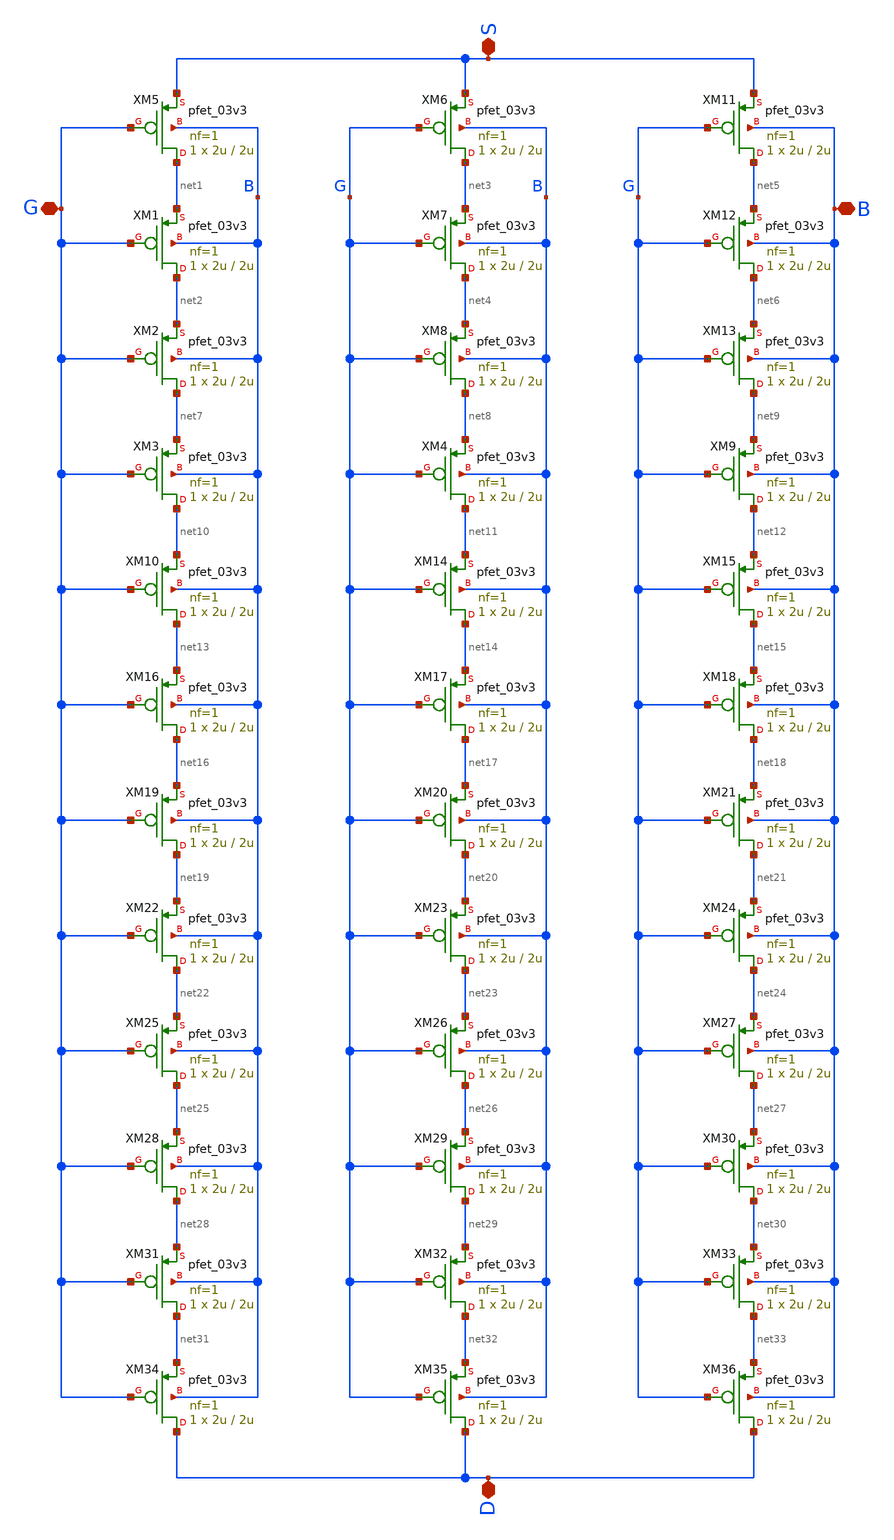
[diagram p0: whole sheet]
** sch_path: Voltage_Reference/symbols_vr/PMOS_matrix_CM2.sch
**.subckt PMOS_matrix_CM2 B G S D
*.iopin B
*.iopin G
*.iopin S
*.iopin D
XM5 net1 G S B pfet_03v3 L=2u W=2u nf=1 ad='int((nf+1)/2) * W/nf * 0.18u' as='int((nf+2)/2) * W/nf * 0.18u'
+ pd='2*int((nf+1)/2) * (W/nf + 0.18u)' ps='2*int((nf+2)/2) * (W/nf + 0.18u)' nrd='0.18u / W' nrs='0.18u / W'
+ sa=0 sb=0 sd=0 m=1
XM1 net2 G net1 B pfet_03v3 L=2u W=2u nf=1 ad='int((nf+1)/2) * W/nf * 0.18u' as='int((nf+2)/2) * W/nf * 0.18u'
+ pd='2*int((nf+1)/2) * (W/nf + 0.18u)' ps='2*int((nf+2)/2) * (W/nf + 0.18u)' nrd='0.18u / W' nrs='0.18u / W'
+ sa=0 sb=0 sd=0 m=1
XM2 net7 G net2 B pfet_03v3 L=2u W=2u nf=1 ad='int((nf+1)/2) * W/nf * 0.18u' as='int((nf+2)/2) * W/nf * 0.18u'
+ pd='2*int((nf+1)/2) * (W/nf + 0.18u)' ps='2*int((nf+2)/2) * (W/nf + 0.18u)' nrd='0.18u / W' nrs='0.18u / W'
+ sa=0 sb=0 sd=0 m=1
XM6 net3 G S B pfet_03v3 L=2u W=2u nf=1 ad='int((nf+1)/2) * W/nf * 0.18u' as='int((nf+2)/2) * W/nf * 0.18u'
+ pd='2*int((nf+1)/2) * (W/nf + 0.18u)' ps='2*int((nf+2)/2) * (W/nf + 0.18u)' nrd='0.18u / W' nrs='0.18u / W'
+ sa=0 sb=0 sd=0 m=1
XM7 net4 G net3 B pfet_03v3 L=2u W=2u nf=1 ad='int((nf+1)/2) * W/nf * 0.18u' as='int((nf+2)/2) * W/nf * 0.18u'
+ pd='2*int((nf+1)/2) * (W/nf + 0.18u)' ps='2*int((nf+2)/2) * (W/nf + 0.18u)' nrd='0.18u / W' nrs='0.18u / W'
+ sa=0 sb=0 sd=0 m=1
XM8 net8 G net4 B pfet_03v3 L=2u W=2u nf=1 ad='int((nf+1)/2) * W/nf * 0.18u' as='int((nf+2)/2) * W/nf * 0.18u'
+ pd='2*int((nf+1)/2) * (W/nf + 0.18u)' ps='2*int((nf+2)/2) * (W/nf + 0.18u)' nrd='0.18u / W' nrs='0.18u / W'
+ sa=0 sb=0 sd=0 m=1
XM11 net5 G S B pfet_03v3 L=2u W=2u nf=1 ad='int((nf+1)/2) * W/nf * 0.18u' as='int((nf+2)/2) * W/nf * 0.18u'
+ pd='2*int((nf+1)/2) * (W/nf + 0.18u)' ps='2*int((nf+2)/2) * (W/nf + 0.18u)' nrd='0.18u / W' nrs='0.18u / W'
+ sa=0 sb=0 sd=0 m=1
XM12 net6 G net5 B pfet_03v3 L=2u W=2u nf=1 ad='int((nf+1)/2) * W/nf * 0.18u' as='int((nf+2)/2) * W/nf * 0.18u'
+ pd='2*int((nf+1)/2) * (W/nf + 0.18u)' ps='2*int((nf+2)/2) * (W/nf + 0.18u)' nrd='0.18u / W' nrs='0.18u / W'
+ sa=0 sb=0 sd=0 m=1
XM13 net9 G net6 B pfet_03v3 L=2u W=2u nf=1 ad='int((nf+1)/2) * W/nf * 0.18u' as='int((nf+2)/2) * W/nf * 0.18u'
+ pd='2*int((nf+1)/2) * (W/nf + 0.18u)' ps='2*int((nf+2)/2) * (W/nf + 0.18u)' nrd='0.18u / W' nrs='0.18u / W'
+ sa=0 sb=0 sd=0 m=1
XM3 net10 G net7 B pfet_03v3 L=2u W=2u nf=1 ad='int((nf+1)/2) * W/nf * 0.18u' as='int((nf+2)/2) * W/nf * 0.18u'
+ pd='2*int((nf+1)/2) * (W/nf + 0.18u)' ps='2*int((nf+2)/2) * (W/nf + 0.18u)' nrd='0.18u / W' nrs='0.18u / W'
+ sa=0 sb=0 sd=0 m=1
XM4 net11 G net8 B pfet_03v3 L=2u W=2u nf=1 ad='int((nf+1)/2) * W/nf * 0.18u' as='int((nf+2)/2) * W/nf * 0.18u'
+ pd='2*int((nf+1)/2) * (W/nf + 0.18u)' ps='2*int((nf+2)/2) * (W/nf + 0.18u)' nrd='0.18u / W' nrs='0.18u / W'
+ sa=0 sb=0 sd=0 m=1
XM9 net12 G net9 B pfet_03v3 L=2u W=2u nf=1 ad='int((nf+1)/2) * W/nf * 0.18u' as='int((nf+2)/2) * W/nf * 0.18u'
+ pd='2*int((nf+1)/2) * (W/nf + 0.18u)' ps='2*int((nf+2)/2) * (W/nf + 0.18u)' nrd='0.18u / W' nrs='0.18u / W'
+ sa=0 sb=0 sd=0 m=1
XM10 net13 G net10 B pfet_03v3 L=2u W=2u nf=1 ad='int((nf+1)/2) * W/nf * 0.18u' as='int((nf+2)/2) * W/nf * 0.18u'
+ pd='2*int((nf+1)/2) * (W/nf + 0.18u)' ps='2*int((nf+2)/2) * (W/nf + 0.18u)' nrd='0.18u / W' nrs='0.18u / W'
+ sa=0 sb=0 sd=0 m=1
XM14 net14 G net11 B pfet_03v3 L=2u W=2u nf=1 ad='int((nf+1)/2) * W/nf * 0.18u' as='int((nf+2)/2) * W/nf * 0.18u'
+ pd='2*int((nf+1)/2) * (W/nf + 0.18u)' ps='2*int((nf+2)/2) * (W/nf + 0.18u)' nrd='0.18u / W' nrs='0.18u / W'
+ sa=0 sb=0 sd=0 m=1
XM15 net15 G net12 B pfet_03v3 L=2u W=2u nf=1 ad='int((nf+1)/2) * W/nf * 0.18u' as='int((nf+2)/2) * W/nf * 0.18u'
+ pd='2*int((nf+1)/2) * (W/nf + 0.18u)' ps='2*int((nf+2)/2) * (W/nf + 0.18u)' nrd='0.18u / W' nrs='0.18u / W'
+ sa=0 sb=0 sd=0 m=1
XM16 net16 G net13 B pfet_03v3 L=2u W=2u nf=1 ad='int((nf+1)/2) * W/nf * 0.18u' as='int((nf+2)/2) * W/nf * 0.18u'
+ pd='2*int((nf+1)/2) * (W/nf + 0.18u)' ps='2*int((nf+2)/2) * (W/nf + 0.18u)' nrd='0.18u / W' nrs='0.18u / W'
+ sa=0 sb=0 sd=0 m=1
XM17 net17 G net14 B pfet_03v3 L=2u W=2u nf=1 ad='int((nf+1)/2) * W/nf * 0.18u' as='int((nf+2)/2) * W/nf * 0.18u'
+ pd='2*int((nf+1)/2) * (W/nf + 0.18u)' ps='2*int((nf+2)/2) * (W/nf + 0.18u)' nrd='0.18u / W' nrs='0.18u / W'
+ sa=0 sb=0 sd=0 m=1
XM18 net18 G net15 B pfet_03v3 L=2u W=2u nf=1 ad='int((nf+1)/2) * W/nf * 0.18u' as='int((nf+2)/2) * W/nf * 0.18u'
+ pd='2*int((nf+1)/2) * (W/nf + 0.18u)' ps='2*int((nf+2)/2) * (W/nf + 0.18u)' nrd='0.18u / W' nrs='0.18u / W'
+ sa=0 sb=0 sd=0 m=1
XM19 net19 G net16 B pfet_03v3 L=2u W=2u nf=1 ad='int((nf+1)/2) * W/nf * 0.18u' as='int((nf+2)/2) * W/nf * 0.18u'
+ pd='2*int((nf+1)/2) * (W/nf + 0.18u)' ps='2*int((nf+2)/2) * (W/nf + 0.18u)' nrd='0.18u / W' nrs='0.18u / W'
+ sa=0 sb=0 sd=0 m=1
XM20 net20 G net17 B pfet_03v3 L=2u W=2u nf=1 ad='int((nf+1)/2) * W/nf * 0.18u' as='int((nf+2)/2) * W/nf * 0.18u'
+ pd='2*int((nf+1)/2) * (W/nf + 0.18u)' ps='2*int((nf+2)/2) * (W/nf + 0.18u)' nrd='0.18u / W' nrs='0.18u / W'
+ sa=0 sb=0 sd=0 m=1
XM21 net21 G net18 B pfet_03v3 L=2u W=2u nf=1 ad='int((nf+1)/2) * W/nf * 0.18u' as='int((nf+2)/2) * W/nf * 0.18u'
+ pd='2*int((nf+1)/2) * (W/nf + 0.18u)' ps='2*int((nf+2)/2) * (W/nf + 0.18u)' nrd='0.18u / W' nrs='0.18u / W'
+ sa=0 sb=0 sd=0 m=1
XM22 net22 G net19 B pfet_03v3 L=2u W=2u nf=1 ad='int((nf+1)/2) * W/nf * 0.18u' as='int((nf+2)/2) * W/nf * 0.18u'
+ pd='2*int((nf+1)/2) * (W/nf + 0.18u)' ps='2*int((nf+2)/2) * (W/nf + 0.18u)' nrd='0.18u / W' nrs='0.18u / W'
+ sa=0 sb=0 sd=0 m=1
XM23 net23 G net20 B pfet_03v3 L=2u W=2u nf=1 ad='int((nf+1)/2) * W/nf * 0.18u' as='int((nf+2)/2) * W/nf * 0.18u'
+ pd='2*int((nf+1)/2) * (W/nf + 0.18u)' ps='2*int((nf+2)/2) * (W/nf + 0.18u)' nrd='0.18u / W' nrs='0.18u / W'
+ sa=0 sb=0 sd=0 m=1
XM24 net24 G net21 B pfet_03v3 L=2u W=2u nf=1 ad='int((nf+1)/2) * W/nf * 0.18u' as='int((nf+2)/2) * W/nf * 0.18u'
+ pd='2*int((nf+1)/2) * (W/nf + 0.18u)' ps='2*int((nf+2)/2) * (W/nf + 0.18u)' nrd='0.18u / W' nrs='0.18u / W'
+ sa=0 sb=0 sd=0 m=1
XM25 net25 G net22 B pfet_03v3 L=2u W=2u nf=1 ad='int((nf+1)/2) * W/nf * 0.18u' as='int((nf+2)/2) * W/nf * 0.18u'
+ pd='2*int((nf+1)/2) * (W/nf + 0.18u)' ps='2*int((nf+2)/2) * (W/nf + 0.18u)' nrd='0.18u / W' nrs='0.18u / W'
+ sa=0 sb=0 sd=0 m=1
XM26 net26 G net23 B pfet_03v3 L=2u W=2u nf=1 ad='int((nf+1)/2) * W/nf * 0.18u' as='int((nf+2)/2) * W/nf * 0.18u'
+ pd='2*int((nf+1)/2) * (W/nf + 0.18u)' ps='2*int((nf+2)/2) * (W/nf + 0.18u)' nrd='0.18u / W' nrs='0.18u / W'
+ sa=0 sb=0 sd=0 m=1
XM27 net27 G net24 B pfet_03v3 L=2u W=2u nf=1 ad='int((nf+1)/2) * W/nf * 0.18u' as='int((nf+2)/2) * W/nf * 0.18u'
+ pd='2*int((nf+1)/2) * (W/nf + 0.18u)' ps='2*int((nf+2)/2) * (W/nf + 0.18u)' nrd='0.18u / W' nrs='0.18u / W'
+ sa=0 sb=0 sd=0 m=1
XM28 net28 G net25 B pfet_03v3 L=2u W=2u nf=1 ad='int((nf+1)/2) * W/nf * 0.18u' as='int((nf+2)/2) * W/nf * 0.18u'
+ pd='2*int((nf+1)/2) * (W/nf + 0.18u)' ps='2*int((nf+2)/2) * (W/nf + 0.18u)' nrd='0.18u / W' nrs='0.18u / W'
+ sa=0 sb=0 sd=0 m=1
XM29 net29 G net26 B pfet_03v3 L=2u W=2u nf=1 ad='int((nf+1)/2) * W/nf * 0.18u' as='int((nf+2)/2) * W/nf * 0.18u'
+ pd='2*int((nf+1)/2) * (W/nf + 0.18u)' ps='2*int((nf+2)/2) * (W/nf + 0.18u)' nrd='0.18u / W' nrs='0.18u / W'
+ sa=0 sb=0 sd=0 m=1
XM30 net30 G net27 B pfet_03v3 L=2u W=2u nf=1 ad='int((nf+1)/2) * W/nf * 0.18u' as='int((nf+2)/2) * W/nf * 0.18u'
+ pd='2*int((nf+1)/2) * (W/nf + 0.18u)' ps='2*int((nf+2)/2) * (W/nf + 0.18u)' nrd='0.18u / W' nrs='0.18u / W'
+ sa=0 sb=0 sd=0 m=1
XM31 net31 G net28 B pfet_03v3 L=2u W=2u nf=1 ad='int((nf+1)/2) * W/nf * 0.18u' as='int((nf+2)/2) * W/nf * 0.18u'
+ pd='2*int((nf+1)/2) * (W/nf + 0.18u)' ps='2*int((nf+2)/2) * (W/nf + 0.18u)' nrd='0.18u / W' nrs='0.18u / W'
+ sa=0 sb=0 sd=0 m=1
XM32 net32 G net29 B pfet_03v3 L=2u W=2u nf=1 ad='int((nf+1)/2) * W/nf * 0.18u' as='int((nf+2)/2) * W/nf * 0.18u'
+ pd='2*int((nf+1)/2) * (W/nf + 0.18u)' ps='2*int((nf+2)/2) * (W/nf + 0.18u)' nrd='0.18u / W' nrs='0.18u / W'
+ sa=0 sb=0 sd=0 m=1
XM33 net33 G net30 B pfet_03v3 L=2u W=2u nf=1 ad='int((nf+1)/2) * W/nf * 0.18u' as='int((nf+2)/2) * W/nf * 0.18u'
+ pd='2*int((nf+1)/2) * (W/nf + 0.18u)' ps='2*int((nf+2)/2) * (W/nf + 0.18u)' nrd='0.18u / W' nrs='0.18u / W'
+ sa=0 sb=0 sd=0 m=1
XM34 D G net31 B pfet_03v3 L=2u W=2u nf=1 ad='int((nf+1)/2) * W/nf * 0.18u' as='int((nf+2)/2) * W/nf * 0.18u'
+ pd='2*int((nf+1)/2) * (W/nf + 0.18u)' ps='2*int((nf+2)/2) * (W/nf + 0.18u)' nrd='0.18u / W' nrs='0.18u / W'
+ sa=0 sb=0 sd=0 m=1
XM35 D G net32 B pfet_03v3 L=2u W=2u nf=1 ad='int((nf+1)/2) * W/nf * 0.18u' as='int((nf+2)/2) * W/nf * 0.18u'
+ pd='2*int((nf+1)/2) * (W/nf + 0.18u)' ps='2*int((nf+2)/2) * (W/nf + 0.18u)' nrd='0.18u / W' nrs='0.18u / W'
+ sa=0 sb=0 sd=0 m=1
XM36 D G net33 B pfet_03v3 L=2u W=2u nf=1 ad='int((nf+1)/2) * W/nf * 0.18u' as='int((nf+2)/2) * W/nf * 0.18u'
+ pd='2*int((nf+1)/2) * (W/nf + 0.18u)' ps='2*int((nf+2)/2) * (W/nf + 0.18u)' nrd='0.18u / W' nrs='0.18u / W'
+ sa=0 sb=0 sd=0 m=1
**.ends
.end
